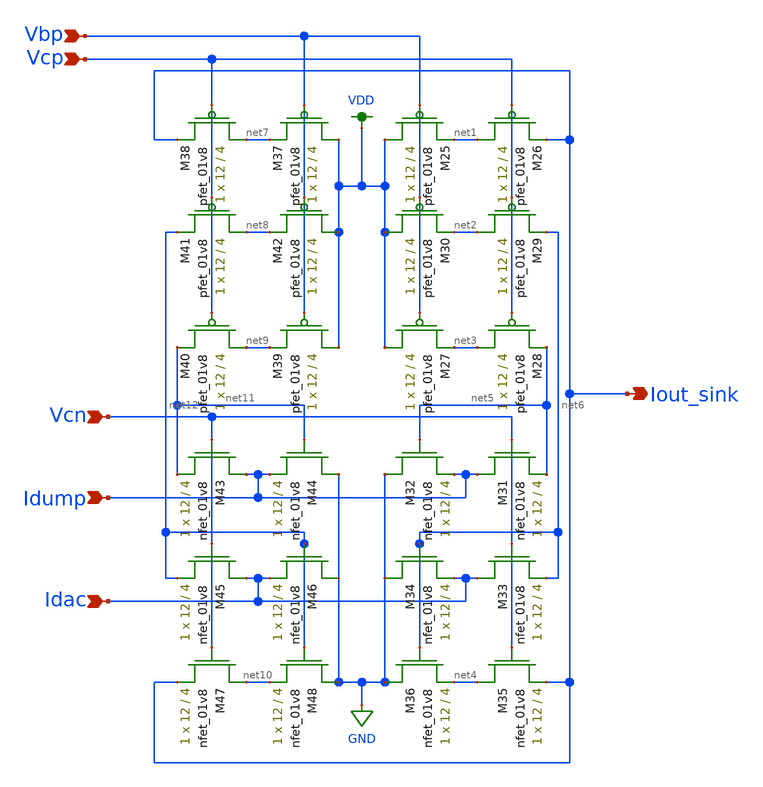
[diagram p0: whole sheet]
** sch_path: modules/output_sink_lds.sch
**.subckt output_sink_lds Iout_sink Vbp Vcp Vcn Idac Idump
*.opin Iout_sink
*.ipin Vbp
*.ipin Vcp
*.ipin Vcn
*.ipin Idac
*.ipin Idump
XM25 VDD Vbp net1 VDD sky130_fd_pr__pfet_01v8 L=4 W=12 nf=1 ad='int((nf+1)/2) * W/nf * 0.29' as='int((nf+2)/2) * W/nf * 0.29'
+ pd='2*int((nf+1)/2) * (W/nf + 0.29)' ps='2*int((nf+2)/2) * (W/nf + 0.29)' nrd='0.29 / W' nrs='0.29 / W'
+ sa=0 sb=0 sd=0 mult=1 m=1
XM26 net1 Vcp Iout_sink VDD sky130_fd_pr__pfet_01v8 L=4 W=12 nf=1 ad='int((nf+1)/2) * W/nf * 0.29' as='int((nf+2)/2) * W/nf * 0.29'
+ pd='2*int((nf+1)/2) * (W/nf + 0.29)' ps='2*int((nf+2)/2) * (W/nf + 0.29)' nrd='0.29 / W' nrs='0.29 / W'
+ sa=0 sb=0 sd=0 mult=1 m=1
XM27 VDD Vbp net3 VDD sky130_fd_pr__pfet_01v8 L=4 W=12 nf=1 ad='int((nf+1)/2) * W/nf * 0.29' as='int((nf+2)/2) * W/nf * 0.29'
+ pd='2*int((nf+1)/2) * (W/nf + 0.29)' ps='2*int((nf+2)/2) * (W/nf + 0.29)' nrd='0.29 / W' nrs='0.29 / W'
+ sa=0 sb=0 sd=0 mult=1 m=1
XM28 net3 Vcp net5 VDD sky130_fd_pr__pfet_01v8 L=4 W=12 nf=1 ad='int((nf+1)/2) * W/nf * 0.29' as='int((nf+2)/2) * W/nf * 0.29'
+ pd='2*int((nf+1)/2) * (W/nf + 0.29)' ps='2*int((nf+2)/2) * (W/nf + 0.29)' nrd='0.29 / W' nrs='0.29 / W'
+ sa=0 sb=0 sd=0 mult=1 m=1
XM29 net2 Vcp net6 VDD sky130_fd_pr__pfet_01v8 L=4 W=12 nf=1 ad='int((nf+1)/2) * W/nf * 0.29' as='int((nf+2)/2) * W/nf * 0.29'
+ pd='2*int((nf+1)/2) * (W/nf + 0.29)' ps='2*int((nf+2)/2) * (W/nf + 0.29)' nrd='0.29 / W' nrs='0.29 / W'
+ sa=0 sb=0 sd=0 mult=1 m=1
XM30 VDD Vbp net2 VDD sky130_fd_pr__pfet_01v8 L=4 W=12 nf=1 ad='int((nf+1)/2) * W/nf * 0.29' as='int((nf+2)/2) * W/nf * 0.29'
+ pd='2*int((nf+1)/2) * (W/nf + 0.29)' ps='2*int((nf+2)/2) * (W/nf + 0.29)' nrd='0.29 / W' nrs='0.29 / W'
+ sa=0 sb=0 sd=0 mult=1 m=1
XM31 Idump Vcn net5 GND sky130_fd_pr__nfet_01v8 L=4 W=12 nf=1 ad='int((nf+1)/2) * W/nf * 0.29' as='int((nf+2)/2) * W/nf * 0.29'
+ pd='2*int((nf+1)/2) * (W/nf + 0.29)' ps='2*int((nf+2)/2) * (W/nf + 0.29)' nrd='0.29 / W' nrs='0.29 / W'
+ sa=0 sb=0 sd=0 mult=1 m=1
XM32 GND net5 Idump GND sky130_fd_pr__nfet_01v8 L=4 W=12 nf=1 ad='int((nf+1)/2) * W/nf * 0.29' as='int((nf+2)/2) * W/nf * 0.29'
+ pd='2*int((nf+1)/2) * (W/nf + 0.29)' ps='2*int((nf+2)/2) * (W/nf + 0.29)' nrd='0.29 / W' nrs='0.29 / W'
+ sa=0 sb=0 sd=0 mult=1 m=1
XM33 Idac Vcn net6 GND sky130_fd_pr__nfet_01v8 L=4 W=12 nf=1 ad='int((nf+1)/2) * W/nf * 0.29' as='int((nf+2)/2) * W/nf * 0.29'
+ pd='2*int((nf+1)/2) * (W/nf + 0.29)' ps='2*int((nf+2)/2) * (W/nf + 0.29)' nrd='0.29 / W' nrs='0.29 / W'
+ sa=0 sb=0 sd=0 mult=1 m=1
XM34 GND net6 Idac GND sky130_fd_pr__nfet_01v8 L=4 W=12 nf=1 ad='int((nf+1)/2) * W/nf * 0.29' as='int((nf+2)/2) * W/nf * 0.29'
+ pd='2*int((nf+1)/2) * (W/nf + 0.29)' ps='2*int((nf+2)/2) * (W/nf + 0.29)' nrd='0.29 / W' nrs='0.29 / W'
+ sa=0 sb=0 sd=0 mult=1 m=1
XM35 net4 Vcn Iout_sink GND sky130_fd_pr__nfet_01v8 L=4 W=12 nf=1 ad='int((nf+1)/2) * W/nf * 0.29' as='int((nf+2)/2) * W/nf * 0.29'
+ pd='2*int((nf+1)/2) * (W/nf + 0.29)' ps='2*int((nf+2)/2) * (W/nf + 0.29)' nrd='0.29 / W' nrs='0.29 / W'
+ sa=0 sb=0 sd=0 mult=1 m=1
XM36 GND net6 net4 GND sky130_fd_pr__nfet_01v8 L=4 W=12 nf=1 ad='int((nf+1)/2) * W/nf * 0.29' as='int((nf+2)/2) * W/nf * 0.29'
+ pd='2*int((nf+1)/2) * (W/nf + 0.29)' ps='2*int((nf+2)/2) * (W/nf + 0.29)' nrd='0.29 / W' nrs='0.29 / W'
+ sa=0 sb=0 sd=0 mult=1 m=1
XM37 VDD Vbp net7 VDD sky130_fd_pr__pfet_01v8 L=4 W=12 nf=1 ad='int((nf+1)/2) * W/nf * 0.29' as='int((nf+2)/2) * W/nf * 0.29'
+ pd='2*int((nf+1)/2) * (W/nf + 0.29)' ps='2*int((nf+2)/2) * (W/nf + 0.29)' nrd='0.29 / W' nrs='0.29 / W'
+ sa=0 sb=0 sd=0 mult=1 m=1
XM38 net7 Vcp Iout_sink VDD sky130_fd_pr__pfet_01v8 L=4 W=12 nf=1 ad='int((nf+1)/2) * W/nf * 0.29' as='int((nf+2)/2) * W/nf * 0.29'
+ pd='2*int((nf+1)/2) * (W/nf + 0.29)' ps='2*int((nf+2)/2) * (W/nf + 0.29)' nrd='0.29 / W' nrs='0.29 / W'
+ sa=0 sb=0 sd=0 mult=1 m=1
XM39 VDD Vbp net9 VDD sky130_fd_pr__pfet_01v8 L=4 W=12 nf=1 ad='int((nf+1)/2) * W/nf * 0.29' as='int((nf+2)/2) * W/nf * 0.29'
+ pd='2*int((nf+1)/2) * (W/nf + 0.29)' ps='2*int((nf+2)/2) * (W/nf + 0.29)' nrd='0.29 / W' nrs='0.29 / W'
+ sa=0 sb=0 sd=0 mult=1 m=1
XM40 net9 Vcp net11 VDD sky130_fd_pr__pfet_01v8 L=4 W=12 nf=1 ad='int((nf+1)/2) * W/nf * 0.29' as='int((nf+2)/2) * W/nf * 0.29'
+ pd='2*int((nf+1)/2) * (W/nf + 0.29)' ps='2*int((nf+2)/2) * (W/nf + 0.29)' nrd='0.29 / W' nrs='0.29 / W'
+ sa=0 sb=0 sd=0 mult=1 m=1
XM41 net8 Vcp net12 VDD sky130_fd_pr__pfet_01v8 L=4 W=12 nf=1 ad='int((nf+1)/2) * W/nf * 0.29' as='int((nf+2)/2) * W/nf * 0.29'
+ pd='2*int((nf+1)/2) * (W/nf + 0.29)' ps='2*int((nf+2)/2) * (W/nf + 0.29)' nrd='0.29 / W' nrs='0.29 / W'
+ sa=0 sb=0 sd=0 mult=1 m=1
XM42 VDD Vbp net8 VDD sky130_fd_pr__pfet_01v8 L=4 W=12 nf=1 ad='int((nf+1)/2) * W/nf * 0.29' as='int((nf+2)/2) * W/nf * 0.29'
+ pd='2*int((nf+1)/2) * (W/nf + 0.29)' ps='2*int((nf+2)/2) * (W/nf + 0.29)' nrd='0.29 / W' nrs='0.29 / W'
+ sa=0 sb=0 sd=0 mult=1 m=1
XM43 Idump Vcn net11 GND sky130_fd_pr__nfet_01v8 L=4 W=12 nf=1 ad='int((nf+1)/2) * W/nf * 0.29' as='int((nf+2)/2) * W/nf * 0.29'
+ pd='2*int((nf+1)/2) * (W/nf + 0.29)' ps='2*int((nf+2)/2) * (W/nf + 0.29)' nrd='0.29 / W' nrs='0.29 / W'
+ sa=0 sb=0 sd=0 mult=1 m=1
XM44 GND net11 Idump GND sky130_fd_pr__nfet_01v8 L=4 W=12 nf=1 ad='int((nf+1)/2) * W/nf * 0.29' as='int((nf+2)/2) * W/nf * 0.29'
+ pd='2*int((nf+1)/2) * (W/nf + 0.29)' ps='2*int((nf+2)/2) * (W/nf + 0.29)' nrd='0.29 / W' nrs='0.29 / W'
+ sa=0 sb=0 sd=0 mult=1 m=1
XM45 Idac Vcn net12 GND sky130_fd_pr__nfet_01v8 L=4 W=12 nf=1 ad='int((nf+1)/2) * W/nf * 0.29' as='int((nf+2)/2) * W/nf * 0.29'
+ pd='2*int((nf+1)/2) * (W/nf + 0.29)' ps='2*int((nf+2)/2) * (W/nf + 0.29)' nrd='0.29 / W' nrs='0.29 / W'
+ sa=0 sb=0 sd=0 mult=1 m=1
XM46 GND net12 Idac GND sky130_fd_pr__nfet_01v8 L=4 W=12 nf=1 ad='int((nf+1)/2) * W/nf * 0.29' as='int((nf+2)/2) * W/nf * 0.29'
+ pd='2*int((nf+1)/2) * (W/nf + 0.29)' ps='2*int((nf+2)/2) * (W/nf + 0.29)' nrd='0.29 / W' nrs='0.29 / W'
+ sa=0 sb=0 sd=0 mult=1 m=1
XM47 net10 Vcn Iout_sink GND sky130_fd_pr__nfet_01v8 L=4 W=12 nf=1 ad='int((nf+1)/2) * W/nf * 0.29' as='int((nf+2)/2) * W/nf * 0.29'
+ pd='2*int((nf+1)/2) * (W/nf + 0.29)' ps='2*int((nf+2)/2) * (W/nf + 0.29)' nrd='0.29 / W' nrs='0.29 / W'
+ sa=0 sb=0 sd=0 mult=1 m=1
XM48 GND net12 net10 GND sky130_fd_pr__nfet_01v8 L=4 W=12 nf=1 ad='int((nf+1)/2) * W/nf * 0.29' as='int((nf+2)/2) * W/nf * 0.29'
+ pd='2*int((nf+1)/2) * (W/nf + 0.29)' ps='2*int((nf+2)/2) * (W/nf + 0.29)' nrd='0.29 / W' nrs='0.29 / W'
+ sa=0 sb=0 sd=0 mult=1 m=1
**.ends
.GLOBAL VDD
.GLOBAL GND
.end
